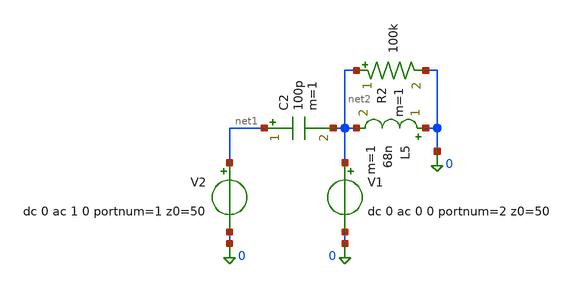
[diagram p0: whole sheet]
** sch_path: tests/SC_Test.sch
**.subckt SC_Test
V2 net1 0 dc 0 ac 1 0 portnum=1 z0=50
V1 net2 0 dc 0 ac 0 0 portnum=2 z0=50
C2 net1 net2 100p m=1
L5 0 net2 68n m=1
R2 net2 0 100k m=1
**** begin user architecture code


.temp 30
.option savecurrents
.save all
.control
  save all

  sp lin 1000 50k 600meg

  remzerovec

  write SC_Test.raw

  *** small-signal AC
  save all
  AC lin 1000 50k 600Meg
  remzerovec
  set appendwrite
  write $inputdir/SC_Test.raw all
  quit 0
.endc




**** end user architecture code
**.ends
.end
